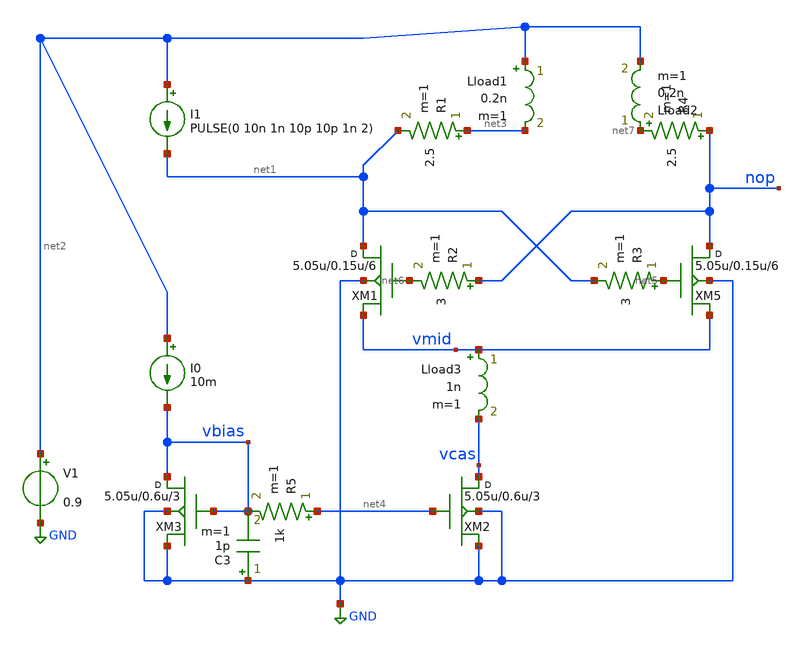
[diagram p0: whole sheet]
** sch_path: xschem/untitled-5.sch
**.subckt untitled-5
XM5 nop net5 vmid GND sky130_fd_pr__rf_nfet_01v8_bM04W5p00L0p15_ext w=5.05u l=0.15u m=6
XM1 net1 net6 vmid GND sky130_fd_pr__rf_nfet_01v8_bM04W5p00L0p15_ext w=5.05u l=0.15u m=6
XM2 vcas net4 GND GND sky130_fd_pr__rf_nfet_01v8_bM04W5p00L0p15_ext w=5.05u l=0.6u m=3
XM3 vbias vbias GND GND sky130_fd_pr__rf_nfet_01v8_bM04W5p00L0p15_ext w=5.05u l=0.6u m=3
I0 net2 vbias 10m
Lload1 net2 net3 0.2n m=1
Lload2 net7 net2 0.2n m=1
V1 net2 GND 0.9
I1 net2 net1 PULSE(0 10n 1n 10p 10p 1n 2)
C3 GND vbias 1p m=1
R2 nop net6 3 m=1
R3 net5 net1 3 m=1
R1 net3 net1 2.5 m=1
R4 nop net7 2.5 m=1
Lload3 vmid vcas 1n m=1
R5 net4 vbias 1k m=1
**** begin user architecture code
.lib $::SKYWATER_MODELS/sky130.lib.spice ff
* .include $::PDKPATH/libs.ref/sky130_fd_sc_hvl/spice/sky130_fd_sc_hvl.spice



.subckt sky130_fd_pr__rf_nfet_01v8_bM04W5p00L0p15_ext DRAIN GATE SOURCE SUBSTRATE
X0 DRAIN GATE SOURCE SUBSTRATE sky130_fd_pr__nfet_01v8 ad=2.828e+12p pd=2.132e+07u as=4.242e+12p
+ ps=3.198e+07u w=5.05e+06u l=150000u
X1 SOURCE SUBSTRATE SUBSTRATE SUBSTRATE sky130_fd_pr__nfet_01v8 ad=0p pd=0u as=3.03e+12p
+ ps=2.14e+07u w=5.05e+06u l=150000u
X2 SOURCE GATE DRAIN SUBSTRATE sky130_fd_pr__nfet_01v8 ad=0p pd=0u as=0p ps=0u w=5.05e+06u l=150000u
X3 DRAIN GATE SOURCE SUBSTRATE sky130_fd_pr__nfet_01v8 ad=0p pd=0u as=0p ps=0u w=5.05e+06u l=150000u
X4 SUBSTRATE SUBSTRATE SOURCE SUBSTRATE sky130_fd_pr__nfet_01v8 ad=0p pd=0u as=0p ps=0u w=5.05e+06u
+ l=150000u
X5 SOURCE GATE DRAIN SUBSTRATE sky130_fd_pr__nfet_01v8 ad=0p pd=0u as=0p ps=0u w=5.05e+06u l=150000u
.ends
.options savecurrents
.tran 1ps 20ns
.control
run
display
plot v(nop)
plot v(nmid)
plot @I1[i]
.endc


**** end user architecture code
**.ends
.GLOBAL GND
.end
